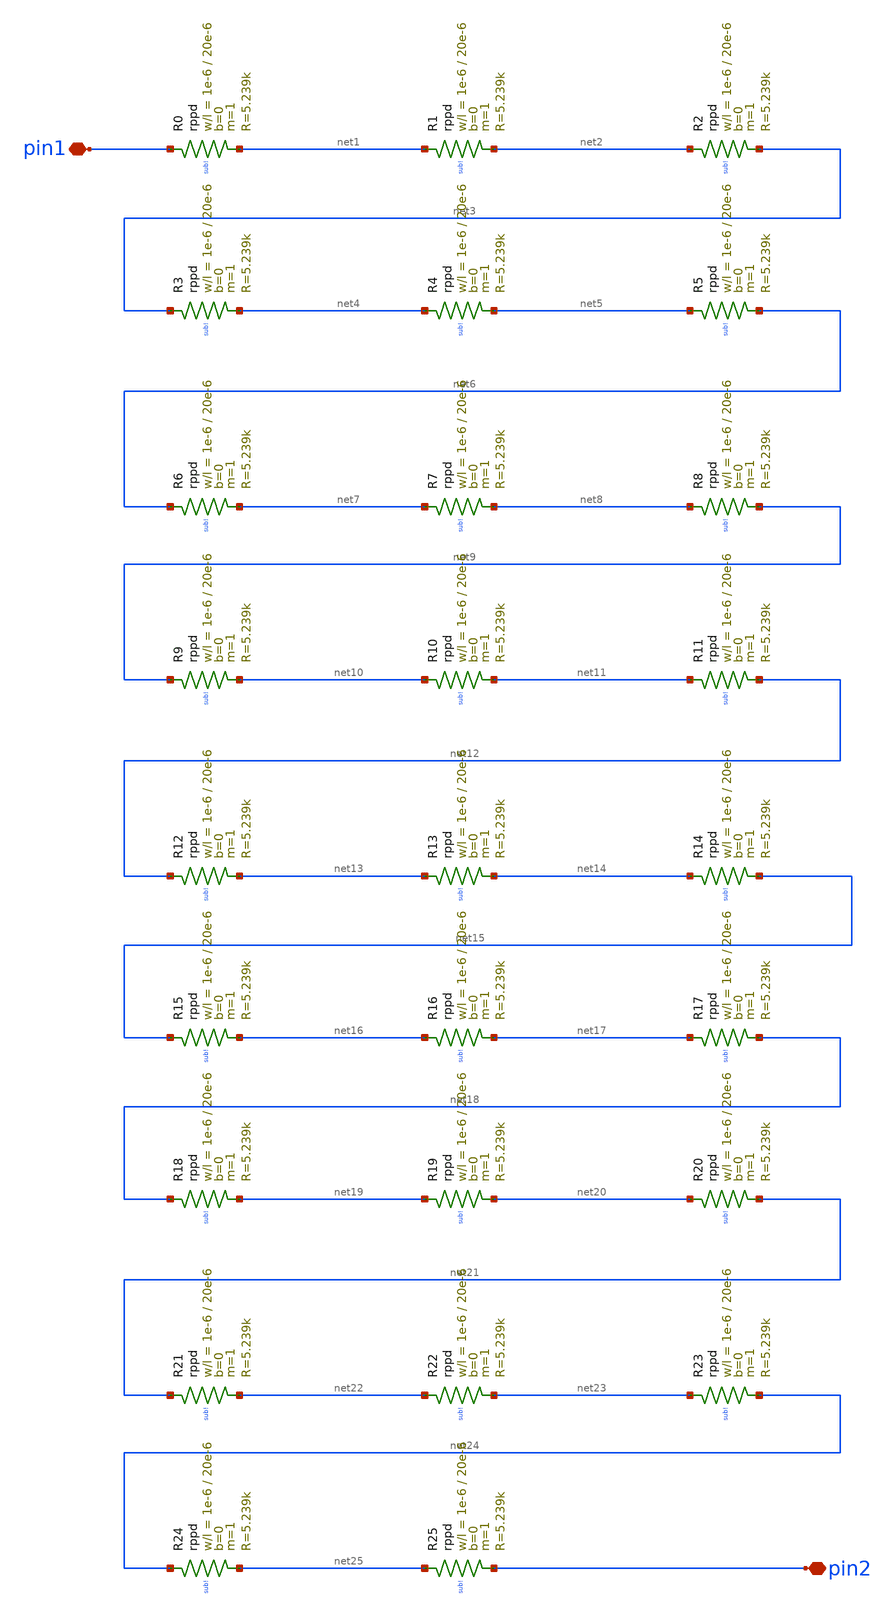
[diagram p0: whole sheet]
** sch_path: ihp-sg13g2/libs.ref/sg13g2_io/sch/xschem/sg13g2_RCClampResistor.sch
**.subckt sg13g2_RCClampResistor pin1 pin2
*.iopin pin1
*.iopin pin2
XR0 pin1 net1 sub! rppd w=1e-6 l=20e-6 m=1 b=0 mm_ok=1
XR1 net1 net2 sub! rppd w=1e-6 l=20e-6 m=1 b=0 mm_ok=1
XR10 net10 net11 sub! rppd w=1e-6 l=20e-6 m=1 b=0 mm_ok=1
XR11 net11 net12 sub! rppd w=1e-6 l=20e-6 m=1 b=0 mm_ok=1
XR12 net12 net13 sub! rppd w=1e-6 l=20e-6 m=1 b=0 mm_ok=1
XR13 net13 net14 sub! rppd w=1e-6 l=20e-6 m=1 b=0 mm_ok=1
XR14 net14 net15 sub! rppd w=1e-6 l=20e-6 m=1 b=0 mm_ok=1
XR15 net15 net16 sub! rppd w=1e-6 l=20e-6 m=1 b=0 mm_ok=1
XR16 net16 net17 sub! rppd w=1e-6 l=20e-6 m=1 b=0 mm_ok=1
XR17 net17 net18 sub! rppd w=1e-6 l=20e-6 m=1 b=0 mm_ok=1
XR18 net18 net19 sub! rppd w=1e-6 l=20e-6 m=1 b=0 mm_ok=1
XR19 net19 net20 sub! rppd w=1e-6 l=20e-6 m=1 b=0 mm_ok=1
XR2 net2 net3 sub! rppd w=1e-6 l=20e-6 m=1 b=0 mm_ok=1
XR20 net20 net21 sub! rppd w=1e-6 l=20e-6 m=1 b=0 mm_ok=1
XR21 net21 net22 sub! rppd w=1e-6 l=20e-6 m=1 b=0 mm_ok=1
XR22 net22 net23 sub! rppd w=1e-6 l=20e-6 m=1 b=0 mm_ok=1
XR23 net23 net24 sub! rppd w=1e-6 l=20e-6 m=1 b=0 mm_ok=1
XR24 net24 net25 sub! rppd w=1e-6 l=20e-6 m=1 b=0 mm_ok=1
XR25 net25 pin2 sub! rppd w=1e-6 l=20e-6 m=1 b=0 mm_ok=1
XR3 net3 net4 sub! rppd w=1e-6 l=20e-6 m=1 b=0 mm_ok=1
XR4 net4 net5 sub! rppd w=1e-6 l=20e-6 m=1 b=0 mm_ok=1
XR5 net5 net6 sub! rppd w=1e-6 l=20e-6 m=1 b=0 mm_ok=1
XR6 net6 net7 sub! rppd w=1e-6 l=20e-6 m=1 b=0 mm_ok=1
XR7 net7 net8 sub! rppd w=1e-6 l=20e-6 m=1 b=0 mm_ok=1
XR8 net8 net9 sub! rppd w=1e-6 l=20e-6 m=1 b=0 mm_ok=1
XR9 net9 net10 sub! rppd w=1e-6 l=20e-6 m=1 b=0 mm_ok=1
**.ends
.end
